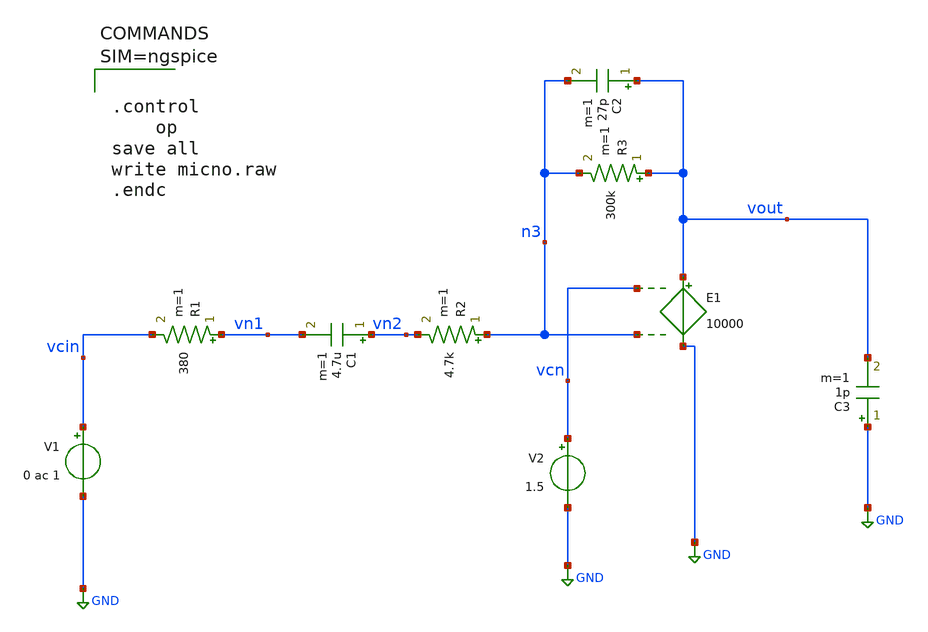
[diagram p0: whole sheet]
** sch_path: micno.sch
**.subckt micno
V1 vcin GND 0 ac 1
R1 vn1 vcin 380 m=1
C1 vn2 vn1 4.7u m=1
R2 n3 vn2 4.7k m=1
C2 vout n3 27p m=1
R3 vout n3 300k m=1
E1 vout GND vcn n3 10000
V2 vcn GND 1.5
C3 GND vout 1p m=1
**** begin user architecture code



.control
	op
save all
write micno.raw
.endc



**** end user architecture code
**.ends
.GLOBAL GND
.end
